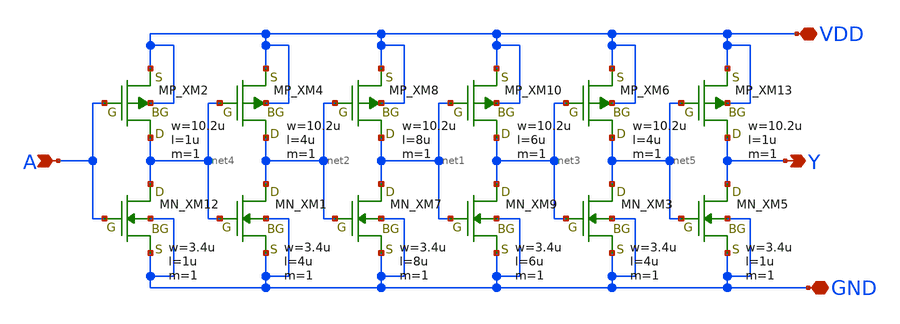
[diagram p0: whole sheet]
** sch_path: openIP62_rev1.0/IP62/Technology/tech/symbols/Xschem/IP62_5_stdcell/DEL2.sch
**.subckt DEL2 A Y VDD GND
*.ipin A
*.opin Y
*.iopin VDD
*.iopin GND
XM13 Y net5 VDD VDD PMOS w=10.2u l=1u as=0 ad=0 ps=0 pd=0 nrd=0 nrs=0 m=1
XM2 net4 A VDD VDD PMOS w=10.2u l=1u as=0 ad=0 ps=0 pd=0 nrd=0 nrs=0 m=1
XM4 net2 net4 VDD VDD PMOS w=10.2u l=4u as=0 ad=0 ps=0 pd=0 nrd=0 nrs=0 m=1
XM6 net5 net3 VDD VDD PMOS w=10.2u l=4u as=0 ad=0 ps=0 pd=0 nrd=0 nrs=0 m=1
XM8 net1 net2 VDD VDD PMOS w=10.2u l=8u as=0 ad=0 ps=0 pd=0 nrd=0 nrs=0 m=1
XM10 net3 net1 VDD VDD PMOS w=10.2u l=6u as=0 ad=0 ps=0 pd=0 nrd=0 nrs=0 m=1
XM12 net4 A GND GND NMOS w=3.4u l=1u as=0 ad=0 ps=0 pd=0 nrd=0 nrs=0 m=1
XM5 Y net5 GND GND NMOS w=3.4u l=1u as=0 ad=0 ps=0 pd=0 nrd=0 nrs=0 m=1
XM1 net2 net4 GND GND NMOS w=3.4u l=4u as=0 ad=0 ps=0 pd=0 nrd=0 nrs=0 m=1
XM3 net5 net3 GND GND NMOS w=3.4u l=4u as=0 ad=0 ps=0 pd=0 nrd=0 nrs=0 m=1
XM7 net1 net2 GND GND NMOS w=3.4u l=8u as=0 ad=0 ps=0 pd=0 nrd=0 nrs=0 m=1
XM9 net3 net1 GND GND NMOS w=3.4u l=6u as=0 ad=0 ps=0 pd=0 nrd=0 nrs=0 m=1
**.ends
.end
